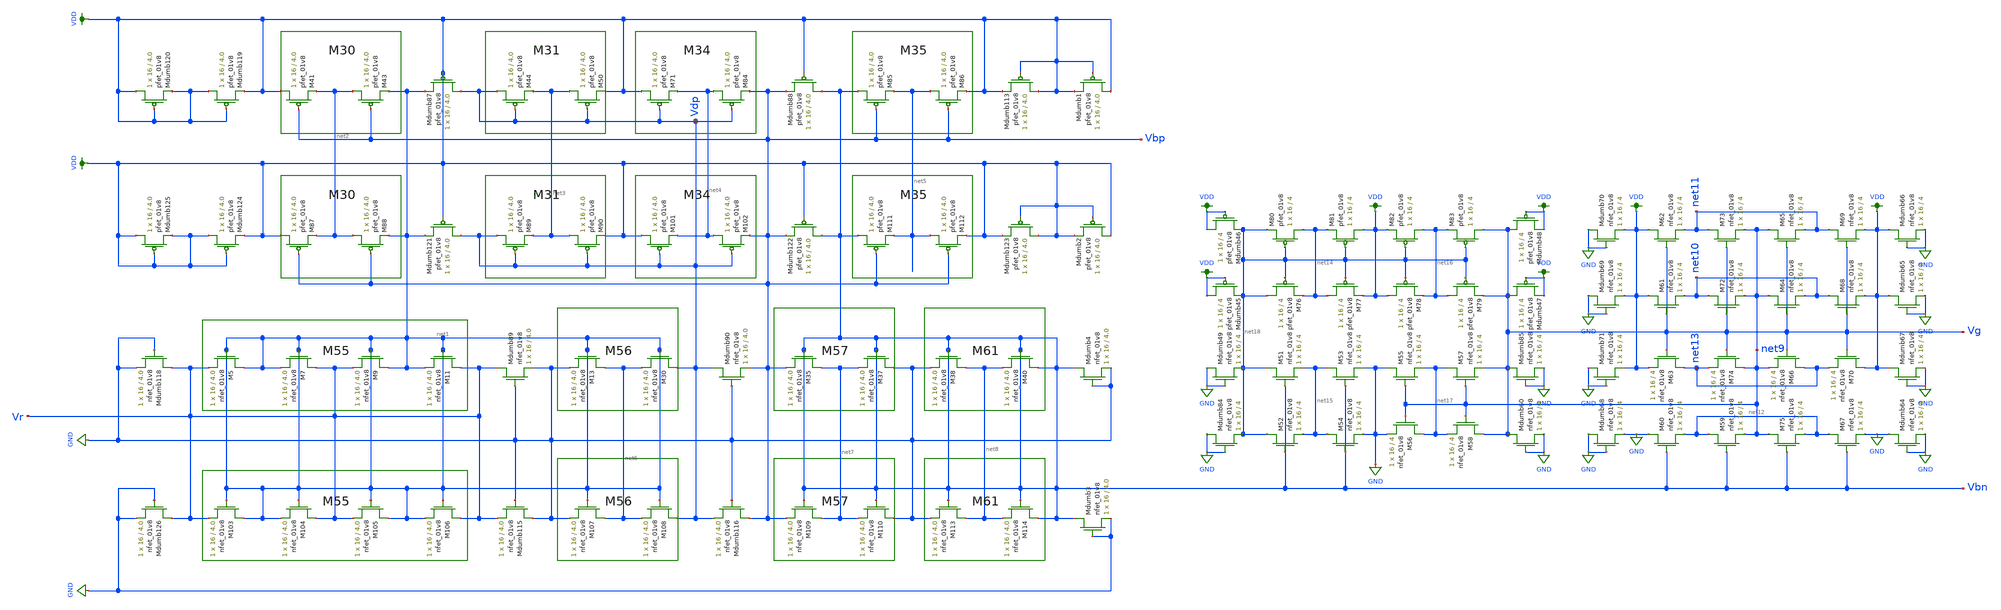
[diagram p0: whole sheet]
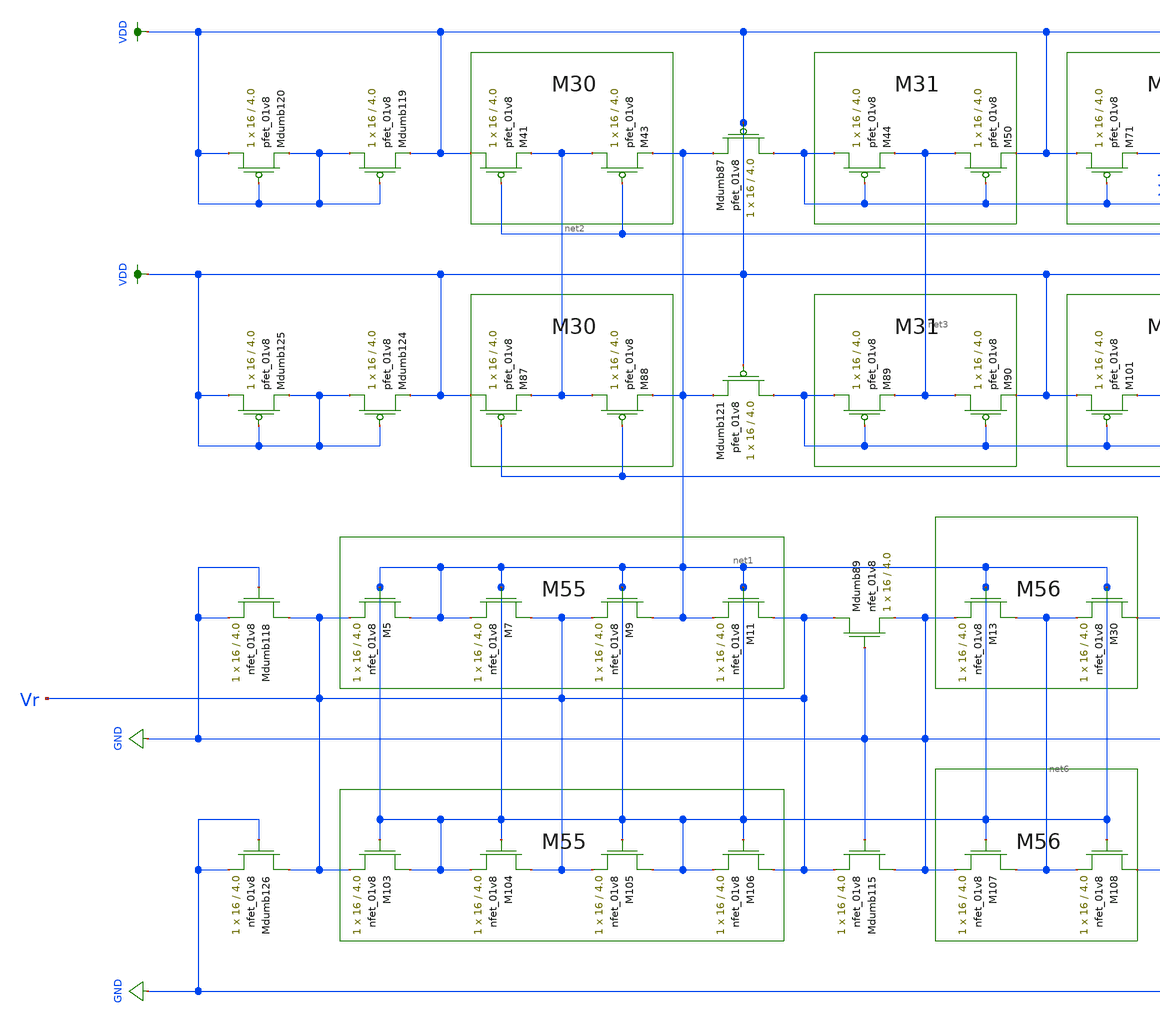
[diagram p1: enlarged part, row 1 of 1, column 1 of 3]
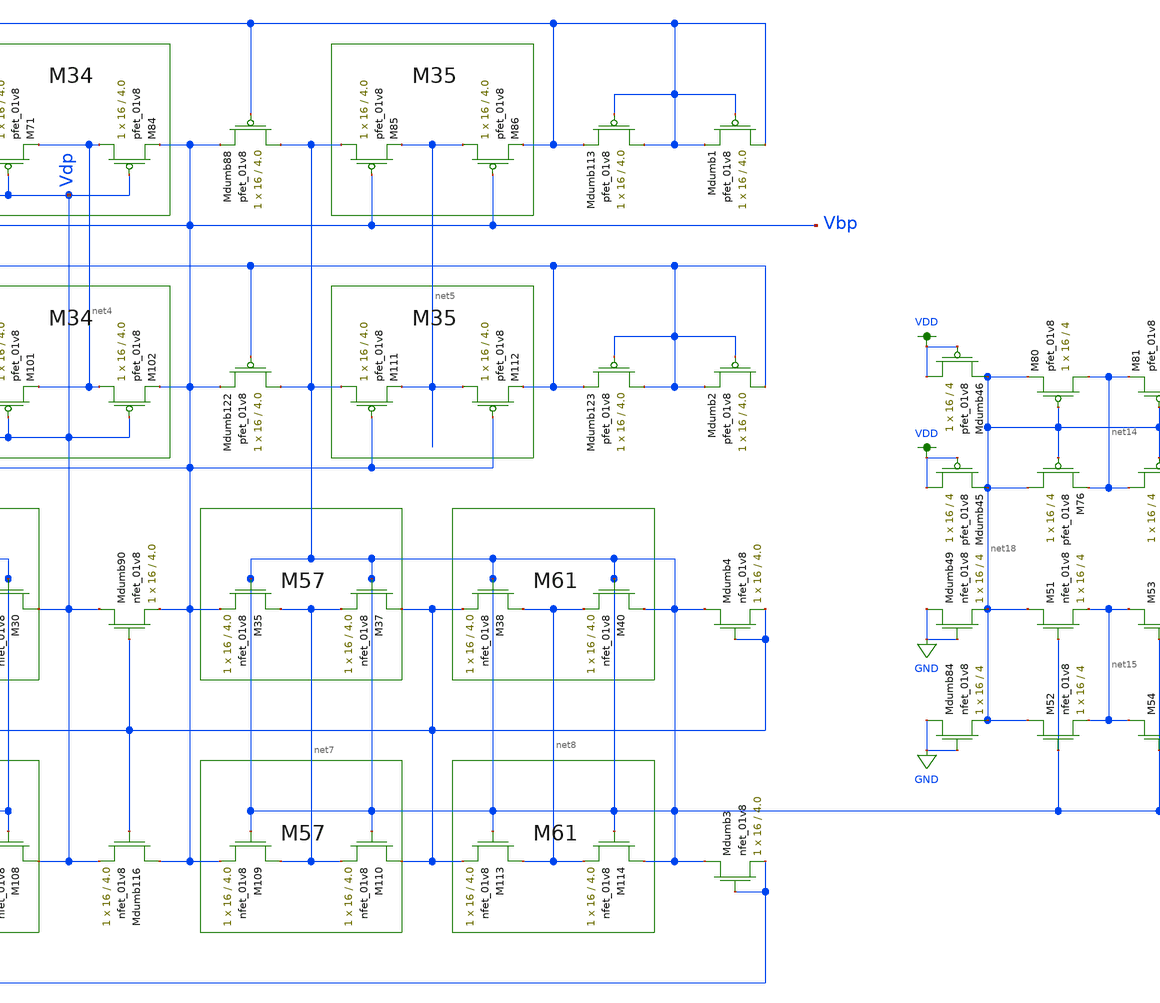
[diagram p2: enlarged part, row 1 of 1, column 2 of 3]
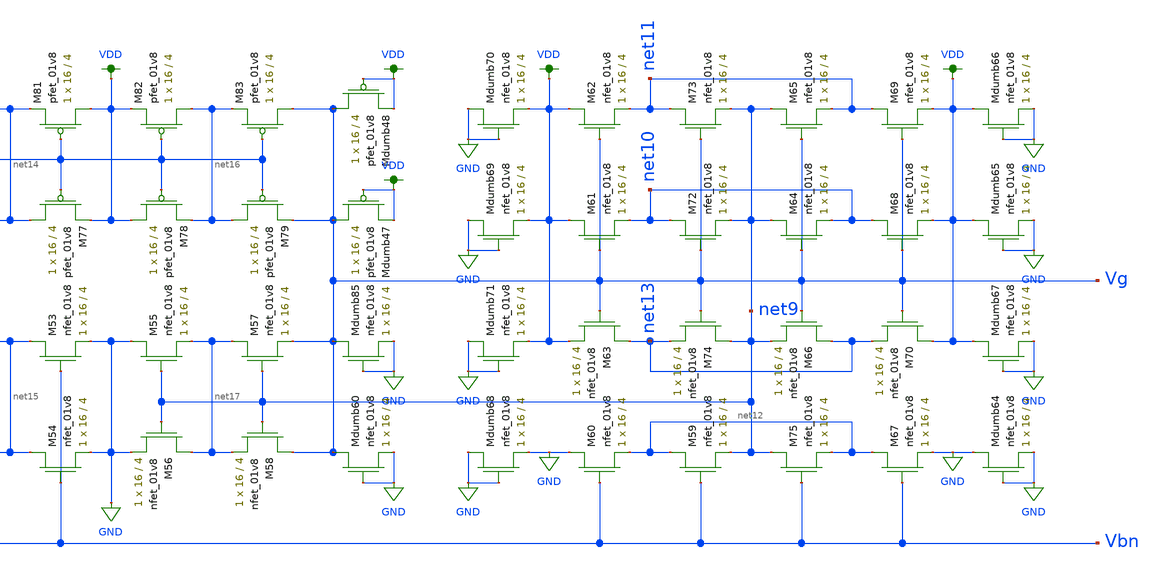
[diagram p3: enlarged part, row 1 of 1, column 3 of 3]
** sch_path: schematic/LDS/ibias_vg_lvs.sch
**.subckt ibias_vg_lvs
XM5 net1 net1 Vr GND sky130_fd_pr__nfet_01v8 L=4.0 W=16 nf=1 ad='int((nf+1)/2) * W/nf * 0.29' as='int((nf+2)/2) * W/nf * 0.29'
+ pd='2*int((nf+1)/2) * (W/nf + 0.29)' ps='2*int((nf+2)/2) * (W/nf + 0.29)' nrd='0.29 / W' nrs='0.29 / W'
+ sa=0 sb=0 sd=0 mult=1 m=1
XM7 Vr net1 net1 GND sky130_fd_pr__nfet_01v8 L=4.0 W=16 nf=1 ad='int((nf+1)/2) * W/nf * 0.29' as='int((nf+2)/2) * W/nf * 0.29'
+ pd='2*int((nf+1)/2) * (W/nf + 0.29)' ps='2*int((nf+2)/2) * (W/nf + 0.29)' nrd='0.29 / W' nrs='0.29 / W'
+ sa=0 sb=0 sd=0 mult=1 m=1
XM9 net1 net1 Vr GND sky130_fd_pr__nfet_01v8 L=4.0 W=16 nf=1 ad='int((nf+1)/2) * W/nf * 0.29' as='int((nf+2)/2) * W/nf * 0.29'
+ pd='2*int((nf+1)/2) * (W/nf + 0.29)' ps='2*int((nf+2)/2) * (W/nf + 0.29)' nrd='0.29 / W' nrs='0.29 / W'
+ sa=0 sb=0 sd=0 mult=1 m=1
XM11 Vr net1 net1 GND sky130_fd_pr__nfet_01v8 L=4.0 W=16 nf=1 ad='int((nf+1)/2) * W/nf * 0.29' as='int((nf+2)/2) * W/nf * 0.29'
+ pd='2*int((nf+1)/2) * (W/nf + 0.29)' ps='2*int((nf+2)/2) * (W/nf + 0.29)' nrd='0.29 / W' nrs='0.29 / W'
+ sa=0 sb=0 sd=0 mult=1 m=1
XM13 net6 net1 GND GND sky130_fd_pr__nfet_01v8 L=4.0 W=16 nf=1 ad='int((nf+1)/2) * W/nf * 0.29' as='int((nf+2)/2) * W/nf * 0.29'
+ pd='2*int((nf+1)/2) * (W/nf + 0.29)' ps='2*int((nf+2)/2) * (W/nf + 0.29)' nrd='0.29 / W' nrs='0.29 / W'
+ sa=0 sb=0 sd=0 mult=1 m=1
XM30 Vdp net1 net6 GND sky130_fd_pr__nfet_01v8 L=4.0 W=16 nf=1 ad='int((nf+1)/2) * W/nf * 0.29' as='int((nf+2)/2) * W/nf * 0.29'
+ pd='2*int((nf+1)/2) * (W/nf + 0.29)' ps='2*int((nf+2)/2) * (W/nf + 0.29)' nrd='0.29 / W' nrs='0.29 / W'
+ sa=0 sb=0 sd=0 mult=1 m=1
XM35 net7 Vbn Vbp GND sky130_fd_pr__nfet_01v8 L=4.0 W=16 nf=1 ad='int((nf+1)/2) * W/nf * 0.29' as='int((nf+2)/2) * W/nf * 0.29'
+ pd='2*int((nf+1)/2) * (W/nf + 0.29)' ps='2*int((nf+2)/2) * (W/nf + 0.29)' nrd='0.29 / W' nrs='0.29 / W'
+ sa=0 sb=0 sd=0 mult=1 m=1
XM37 GND Vbn net7 GND sky130_fd_pr__nfet_01v8 L=4.0 W=16 nf=1 ad='int((nf+1)/2) * W/nf * 0.29' as='int((nf+2)/2) * W/nf * 0.29'
+ pd='2*int((nf+1)/2) * (W/nf + 0.29)' ps='2*int((nf+2)/2) * (W/nf + 0.29)' nrd='0.29 / W' nrs='0.29 / W'
+ sa=0 sb=0 sd=0 mult=1 m=1
XM38 net8 Vbn GND GND sky130_fd_pr__nfet_01v8 L=4.0 W=16 nf=1 ad='int((nf+1)/2) * W/nf * 0.29' as='int((nf+2)/2) * W/nf * 0.29'
+ pd='2*int((nf+1)/2) * (W/nf + 0.29)' ps='2*int((nf+2)/2) * (W/nf + 0.29)' nrd='0.29 / W' nrs='0.29 / W'
+ sa=0 sb=0 sd=0 mult=1 m=1
XM40 Vbn Vbn net8 GND sky130_fd_pr__nfet_01v8 L=4.0 W=16 nf=1 ad='int((nf+1)/2) * W/nf * 0.29' as='int((nf+2)/2) * W/nf * 0.29'
+ pd='2*int((nf+1)/2) * (W/nf + 0.29)' ps='2*int((nf+2)/2) * (W/nf + 0.29)' nrd='0.29 / W' nrs='0.29 / W'
+ sa=0 sb=0 sd=0 mult=1 m=1
XM41 VDD Vbp net2 VDD sky130_fd_pr__pfet_01v8 L=4.0 W=16 nf=1 ad='int((nf+1)/2) * W/nf * 0.29' as='int((nf+2)/2) * W/nf * 0.29'
+ pd='2*int((nf+1)/2) * (W/nf + 0.29)' ps='2*int((nf+2)/2) * (W/nf + 0.29)' nrd='0.29 / W' nrs='0.29 / W'
+ sa=0 sb=0 sd=0 mult=1 m=1
XM43 net2 Vbp net1 VDD sky130_fd_pr__pfet_01v8 L=4.0 W=16 nf=1 ad='int((nf+1)/2) * W/nf * 0.29' as='int((nf+2)/2) * W/nf * 0.29'
+ pd='2*int((nf+1)/2) * (W/nf + 0.29)' ps='2*int((nf+2)/2) * (W/nf + 0.29)' nrd='0.29 / W' nrs='0.29 / W'
+ sa=0 sb=0 sd=0 mult=1 m=1
XM44 Vdp Vdp net3 VDD sky130_fd_pr__pfet_01v8 L=4.0 W=16 nf=1 ad='int((nf+1)/2) * W/nf * 0.29' as='int((nf+2)/2) * W/nf * 0.29'
+ pd='2*int((nf+1)/2) * (W/nf + 0.29)' ps='2*int((nf+2)/2) * (W/nf + 0.29)' nrd='0.29 / W' nrs='0.29 / W'
+ sa=0 sb=0 sd=0 mult=1 m=1
XM50 net3 Vdp VDD VDD sky130_fd_pr__pfet_01v8 L=4.0 W=16 nf=1 ad='int((nf+1)/2) * W/nf * 0.29' as='int((nf+2)/2) * W/nf * 0.29'
+ pd='2*int((nf+1)/2) * (W/nf + 0.29)' ps='2*int((nf+2)/2) * (W/nf + 0.29)' nrd='0.29 / W' nrs='0.29 / W'
+ sa=0 sb=0 sd=0 mult=1 m=1
XM71 VDD Vdp net4 VDD sky130_fd_pr__pfet_01v8 L=4.0 W=16 nf=1 ad='int((nf+1)/2) * W/nf * 0.29' as='int((nf+2)/2) * W/nf * 0.29'
+ pd='2*int((nf+1)/2) * (W/nf + 0.29)' ps='2*int((nf+2)/2) * (W/nf + 0.29)' nrd='0.29 / W' nrs='0.29 / W'
+ sa=0 sb=0 sd=0 mult=1 m=1
XM84 net4 Vdp Vbp VDD sky130_fd_pr__pfet_01v8 L=4.0 W=16 nf=1 ad='int((nf+1)/2) * W/nf * 0.29' as='int((nf+2)/2) * W/nf * 0.29'
+ pd='2*int((nf+1)/2) * (W/nf + 0.29)' ps='2*int((nf+2)/2) * (W/nf + 0.29)' nrd='0.29 / W' nrs='0.29 / W'
+ sa=0 sb=0 sd=0 mult=1 m=1
XM85 Vbn Vbp net5 VDD sky130_fd_pr__pfet_01v8 L=4.0 W=16 nf=1 ad='int((nf+1)/2) * W/nf * 0.29' as='int((nf+2)/2) * W/nf * 0.29'
+ pd='2*int((nf+1)/2) * (W/nf + 0.29)' ps='2*int((nf+2)/2) * (W/nf + 0.29)' nrd='0.29 / W' nrs='0.29 / W'
+ sa=0 sb=0 sd=0 mult=1 m=1
XM86 net5 Vbp VDD VDD sky130_fd_pr__pfet_01v8 L=4.0 W=16 nf=1 ad='int((nf+1)/2) * W/nf * 0.29' as='int((nf+2)/2) * W/nf * 0.29'
+ pd='2*int((nf+1)/2) * (W/nf + 0.29)' ps='2*int((nf+2)/2) * (W/nf + 0.29)' nrd='0.29 / W' nrs='0.29 / W'
+ sa=0 sb=0 sd=0 mult=1 m=1
XMdumb87 Vdp VDD net1 VDD sky130_fd_pr__pfet_01v8 L=4.0 W=16 nf=1 ad='int((nf+1)/2) * W/nf * 0.29' as='int((nf+2)/2) * W/nf * 0.29'
+ pd='2*int((nf+1)/2) * (W/nf + 0.29)' ps='2*int((nf+2)/2) * (W/nf + 0.29)' nrd='0.29 / W' nrs='0.29 / W'
+ sa=0 sb=0 sd=0 mult=1 m=1
XMdumb88 Vbn VDD Vbp VDD sky130_fd_pr__pfet_01v8 L=4.0 W=16 nf=1 ad='int((nf+1)/2) * W/nf * 0.29' as='int((nf+2)/2) * W/nf * 0.29'
+ pd='2*int((nf+1)/2) * (W/nf + 0.29)' ps='2*int((nf+2)/2) * (W/nf + 0.29)' nrd='0.29 / W' nrs='0.29 / W'
+ sa=0 sb=0 sd=0 mult=1 m=1
XMdumb89 Vr GND GND GND sky130_fd_pr__nfet_01v8 L=4.0 W=16 nf=1 ad='int((nf+1)/2) * W/nf * 0.29' as='int((nf+2)/2) * W/nf * 0.29'
+ pd='2*int((nf+1)/2) * (W/nf + 0.29)' ps='2*int((nf+2)/2) * (W/nf + 0.29)' nrd='0.29 / W' nrs='0.29 / W'
+ sa=0 sb=0 sd=0 mult=1 m=1
XMdumb90 Vdp GND Vbp GND sky130_fd_pr__nfet_01v8 L=4.0 W=16 nf=1 ad='int((nf+1)/2) * W/nf * 0.29' as='int((nf+2)/2) * W/nf * 0.29'
+ pd='2*int((nf+1)/2) * (W/nf + 0.29)' ps='2*int((nf+2)/2) * (W/nf + 0.29)' nrd='0.29 / W' nrs='0.29 / W'
+ sa=0 sb=0 sd=0 mult=1 m=1
XMdumb113 VDD VDD VDD VDD sky130_fd_pr__pfet_01v8 L=4.0 W=16 nf=1 ad='int((nf+1)/2) * W/nf * 0.29' as='int((nf+2)/2) * W/nf * 0.29'
+ pd='2*int((nf+1)/2) * (W/nf + 0.29)' ps='2*int((nf+2)/2) * (W/nf + 0.29)' nrd='0.29 / W' nrs='0.29 / W'
+ sa=0 sb=0 sd=0 mult=1 m=1
XMdumb118 Vr GND GND GND sky130_fd_pr__nfet_01v8 L=4.0 W=16 nf=1 ad='int((nf+1)/2) * W/nf * 0.29' as='int((nf+2)/2) * W/nf * 0.29'
+ pd='2*int((nf+1)/2) * (W/nf + 0.29)' ps='2*int((nf+2)/2) * (W/nf + 0.29)' nrd='0.29 / W' nrs='0.29 / W'
+ sa=0 sb=0 sd=0 mult=1 m=1
XMdumb119 VDD VDD VDD VDD sky130_fd_pr__pfet_01v8 L=4.0 W=16 nf=1 ad='int((nf+1)/2) * W/nf * 0.29' as='int((nf+2)/2) * W/nf * 0.29'
+ pd='2*int((nf+1)/2) * (W/nf + 0.29)' ps='2*int((nf+2)/2) * (W/nf + 0.29)' nrd='0.29 / W' nrs='0.29 / W'
+ sa=0 sb=0 sd=0 mult=1 m=1
XMdumb120 VDD VDD VDD VDD sky130_fd_pr__pfet_01v8 L=4.0 W=16 nf=1 ad='int((nf+1)/2) * W/nf * 0.29' as='int((nf+2)/2) * W/nf * 0.29'
+ pd='2*int((nf+1)/2) * (W/nf + 0.29)' ps='2*int((nf+2)/2) * (W/nf + 0.29)' nrd='0.29 / W' nrs='0.29 / W'
+ sa=0 sb=0 sd=0 mult=1 m=1
XM87 VDD Vbp net2 VDD sky130_fd_pr__pfet_01v8 L=4.0 W=16 nf=1 ad='int((nf+1)/2) * W/nf * 0.29' as='int((nf+2)/2) * W/nf * 0.29'
+ pd='2*int((nf+1)/2) * (W/nf + 0.29)' ps='2*int((nf+2)/2) * (W/nf + 0.29)' nrd='0.29 / W' nrs='0.29 / W'
+ sa=0 sb=0 sd=0 mult=1 m=1
XM88 net2 Vbp net1 VDD sky130_fd_pr__pfet_01v8 L=4.0 W=16 nf=1 ad='int((nf+1)/2) * W/nf * 0.29' as='int((nf+2)/2) * W/nf * 0.29'
+ pd='2*int((nf+1)/2) * (W/nf + 0.29)' ps='2*int((nf+2)/2) * (W/nf + 0.29)' nrd='0.29 / W' nrs='0.29 / W'
+ sa=0 sb=0 sd=0 mult=1 m=1
XM89 Vdp Vdp net3 VDD sky130_fd_pr__pfet_01v8 L=4.0 W=16 nf=1 ad='int((nf+1)/2) * W/nf * 0.29' as='int((nf+2)/2) * W/nf * 0.29'
+ pd='2*int((nf+1)/2) * (W/nf + 0.29)' ps='2*int((nf+2)/2) * (W/nf + 0.29)' nrd='0.29 / W' nrs='0.29 / W'
+ sa=0 sb=0 sd=0 mult=1 m=1
XM90 net3 Vdp VDD VDD sky130_fd_pr__pfet_01v8 L=4.0 W=16 nf=1 ad='int((nf+1)/2) * W/nf * 0.29' as='int((nf+2)/2) * W/nf * 0.29'
+ pd='2*int((nf+1)/2) * (W/nf + 0.29)' ps='2*int((nf+2)/2) * (W/nf + 0.29)' nrd='0.29 / W' nrs='0.29 / W'
+ sa=0 sb=0 sd=0 mult=1 m=1
XM101 VDD Vdp net4 VDD sky130_fd_pr__pfet_01v8 L=4.0 W=16 nf=1 ad='int((nf+1)/2) * W/nf * 0.29' as='int((nf+2)/2) * W/nf * 0.29'
+ pd='2*int((nf+1)/2) * (W/nf + 0.29)' ps='2*int((nf+2)/2) * (W/nf + 0.29)' nrd='0.29 / W' nrs='0.29 / W'
+ sa=0 sb=0 sd=0 mult=1 m=1
XM102 net4 Vdp Vbp VDD sky130_fd_pr__pfet_01v8 L=4.0 W=16 nf=1 ad='int((nf+1)/2) * W/nf * 0.29' as='int((nf+2)/2) * W/nf * 0.29'
+ pd='2*int((nf+1)/2) * (W/nf + 0.29)' ps='2*int((nf+2)/2) * (W/nf + 0.29)' nrd='0.29 / W' nrs='0.29 / W'
+ sa=0 sb=0 sd=0 mult=1 m=1
XM111 Vbn Vbp net5 VDD sky130_fd_pr__pfet_01v8 L=4.0 W=16 nf=1 ad='int((nf+1)/2) * W/nf * 0.29' as='int((nf+2)/2) * W/nf * 0.29'
+ pd='2*int((nf+1)/2) * (W/nf + 0.29)' ps='2*int((nf+2)/2) * (W/nf + 0.29)' nrd='0.29 / W' nrs='0.29 / W'
+ sa=0 sb=0 sd=0 mult=1 m=1
XM112 net5 Vbp VDD VDD sky130_fd_pr__pfet_01v8 L=4.0 W=16 nf=1 ad='int((nf+1)/2) * W/nf * 0.29' as='int((nf+2)/2) * W/nf * 0.29'
+ pd='2*int((nf+1)/2) * (W/nf + 0.29)' ps='2*int((nf+2)/2) * (W/nf + 0.29)' nrd='0.29 / W' nrs='0.29 / W'
+ sa=0 sb=0 sd=0 mult=1 m=1
XMdumb121 Vdp VDD net1 VDD sky130_fd_pr__pfet_01v8 L=4.0 W=16 nf=1 ad='int((nf+1)/2) * W/nf * 0.29' as='int((nf+2)/2) * W/nf * 0.29'
+ pd='2*int((nf+1)/2) * (W/nf + 0.29)' ps='2*int((nf+2)/2) * (W/nf + 0.29)' nrd='0.29 / W' nrs='0.29 / W'
+ sa=0 sb=0 sd=0 mult=1 m=1
XMdumb122 Vbn VDD Vbp VDD sky130_fd_pr__pfet_01v8 L=4.0 W=16 nf=1 ad='int((nf+1)/2) * W/nf * 0.29' as='int((nf+2)/2) * W/nf * 0.29'
+ pd='2*int((nf+1)/2) * (W/nf + 0.29)' ps='2*int((nf+2)/2) * (W/nf + 0.29)' nrd='0.29 / W' nrs='0.29 / W'
+ sa=0 sb=0 sd=0 mult=1 m=1
XMdumb123 VDD VDD VDD VDD sky130_fd_pr__pfet_01v8 L=4.0 W=16 nf=1 ad='int((nf+1)/2) * W/nf * 0.29' as='int((nf+2)/2) * W/nf * 0.29'
+ pd='2*int((nf+1)/2) * (W/nf + 0.29)' ps='2*int((nf+2)/2) * (W/nf + 0.29)' nrd='0.29 / W' nrs='0.29 / W'
+ sa=0 sb=0 sd=0 mult=1 m=1
XMdumb124 VDD VDD VDD VDD sky130_fd_pr__pfet_01v8 L=4.0 W=16 nf=1 ad='int((nf+1)/2) * W/nf * 0.29' as='int((nf+2)/2) * W/nf * 0.29'
+ pd='2*int((nf+1)/2) * (W/nf + 0.29)' ps='2*int((nf+2)/2) * (W/nf + 0.29)' nrd='0.29 / W' nrs='0.29 / W'
+ sa=0 sb=0 sd=0 mult=1 m=1
XMdumb125 VDD VDD VDD VDD sky130_fd_pr__pfet_01v8 L=4.0 W=16 nf=1 ad='int((nf+1)/2) * W/nf * 0.29' as='int((nf+2)/2) * W/nf * 0.29'
+ pd='2*int((nf+1)/2) * (W/nf + 0.29)' ps='2*int((nf+2)/2) * (W/nf + 0.29)' nrd='0.29 / W' nrs='0.29 / W'
+ sa=0 sb=0 sd=0 mult=1 m=1
XM103 net1 net1 Vr GND sky130_fd_pr__nfet_01v8 L=4.0 W=16 nf=1 ad='int((nf+1)/2) * W/nf * 0.29' as='int((nf+2)/2) * W/nf * 0.29'
+ pd='2*int((nf+1)/2) * (W/nf + 0.29)' ps='2*int((nf+2)/2) * (W/nf + 0.29)' nrd='0.29 / W' nrs='0.29 / W'
+ sa=0 sb=0 sd=0 mult=1 m=1
XM104 Vr net1 net1 GND sky130_fd_pr__nfet_01v8 L=4.0 W=16 nf=1 ad='int((nf+1)/2) * W/nf * 0.29' as='int((nf+2)/2) * W/nf * 0.29'
+ pd='2*int((nf+1)/2) * (W/nf + 0.29)' ps='2*int((nf+2)/2) * (W/nf + 0.29)' nrd='0.29 / W' nrs='0.29 / W'
+ sa=0 sb=0 sd=0 mult=1 m=1
XM105 net1 net1 Vr GND sky130_fd_pr__nfet_01v8 L=4.0 W=16 nf=1 ad='int((nf+1)/2) * W/nf * 0.29' as='int((nf+2)/2) * W/nf * 0.29'
+ pd='2*int((nf+1)/2) * (W/nf + 0.29)' ps='2*int((nf+2)/2) * (W/nf + 0.29)' nrd='0.29 / W' nrs='0.29 / W'
+ sa=0 sb=0 sd=0 mult=1 m=1
XM106 Vr net1 net1 GND sky130_fd_pr__nfet_01v8 L=4.0 W=16 nf=1 ad='int((nf+1)/2) * W/nf * 0.29' as='int((nf+2)/2) * W/nf * 0.29'
+ pd='2*int((nf+1)/2) * (W/nf + 0.29)' ps='2*int((nf+2)/2) * (W/nf + 0.29)' nrd='0.29 / W' nrs='0.29 / W'
+ sa=0 sb=0 sd=0 mult=1 m=1
XM107 net6 net1 GND GND sky130_fd_pr__nfet_01v8 L=4.0 W=16 nf=1 ad='int((nf+1)/2) * W/nf * 0.29' as='int((nf+2)/2) * W/nf * 0.29'
+ pd='2*int((nf+1)/2) * (W/nf + 0.29)' ps='2*int((nf+2)/2) * (W/nf + 0.29)' nrd='0.29 / W' nrs='0.29 / W'
+ sa=0 sb=0 sd=0 mult=1 m=1
XM108 Vdp net1 net6 GND sky130_fd_pr__nfet_01v8 L=4.0 W=16 nf=1 ad='int((nf+1)/2) * W/nf * 0.29' as='int((nf+2)/2) * W/nf * 0.29'
+ pd='2*int((nf+1)/2) * (W/nf + 0.29)' ps='2*int((nf+2)/2) * (W/nf + 0.29)' nrd='0.29 / W' nrs='0.29 / W'
+ sa=0 sb=0 sd=0 mult=1 m=1
XM109 net7 Vbn Vbp GND sky130_fd_pr__nfet_01v8 L=4.0 W=16 nf=1 ad='int((nf+1)/2) * W/nf * 0.29' as='int((nf+2)/2) * W/nf * 0.29'
+ pd='2*int((nf+1)/2) * (W/nf + 0.29)' ps='2*int((nf+2)/2) * (W/nf + 0.29)' nrd='0.29 / W' nrs='0.29 / W'
+ sa=0 sb=0 sd=0 mult=1 m=1
XM110 GND Vbn net7 GND sky130_fd_pr__nfet_01v8 L=4.0 W=16 nf=1 ad='int((nf+1)/2) * W/nf * 0.29' as='int((nf+2)/2) * W/nf * 0.29'
+ pd='2*int((nf+1)/2) * (W/nf + 0.29)' ps='2*int((nf+2)/2) * (W/nf + 0.29)' nrd='0.29 / W' nrs='0.29 / W'
+ sa=0 sb=0 sd=0 mult=1 m=1
XM113 net8 Vbn GND GND sky130_fd_pr__nfet_01v8 L=4.0 W=16 nf=1 ad='int((nf+1)/2) * W/nf * 0.29' as='int((nf+2)/2) * W/nf * 0.29'
+ pd='2*int((nf+1)/2) * (W/nf + 0.29)' ps='2*int((nf+2)/2) * (W/nf + 0.29)' nrd='0.29 / W' nrs='0.29 / W'
+ sa=0 sb=0 sd=0 mult=1 m=1
XM114 Vbn Vbn net8 GND sky130_fd_pr__nfet_01v8 L=4.0 W=16 nf=1 ad='int((nf+1)/2) * W/nf * 0.29' as='int((nf+2)/2) * W/nf * 0.29'
+ pd='2*int((nf+1)/2) * (W/nf + 0.29)' ps='2*int((nf+2)/2) * (W/nf + 0.29)' nrd='0.29 / W' nrs='0.29 / W'
+ sa=0 sb=0 sd=0 mult=1 m=1
XMdumb115 GND GND Vr GND sky130_fd_pr__nfet_01v8 L=4.0 W=16 nf=1 ad='int((nf+1)/2) * W/nf * 0.29' as='int((nf+2)/2) * W/nf * 0.29'
+ pd='2*int((nf+1)/2) * (W/nf + 0.29)' ps='2*int((nf+2)/2) * (W/nf + 0.29)' nrd='0.29 / W' nrs='0.29 / W'
+ sa=0 sb=0 sd=0 mult=1 m=1
XMdumb116 Vbp GND Vdp GND sky130_fd_pr__nfet_01v8 L=4.0 W=16 nf=1 ad='int((nf+1)/2) * W/nf * 0.29' as='int((nf+2)/2) * W/nf * 0.29'
+ pd='2*int((nf+1)/2) * (W/nf + 0.29)' ps='2*int((nf+2)/2) * (W/nf + 0.29)' nrd='0.29 / W' nrs='0.29 / W'
+ sa=0 sb=0 sd=0 mult=1 m=1
XMdumb126 Vr GND GND GND sky130_fd_pr__nfet_01v8 L=4.0 W=16 nf=1 ad='int((nf+1)/2) * W/nf * 0.29' as='int((nf+2)/2) * W/nf * 0.29'
+ pd='2*int((nf+1)/2) * (W/nf + 0.29)' ps='2*int((nf+2)/2) * (W/nf + 0.29)' nrd='0.29 / W' nrs='0.29 / W'
+ sa=0 sb=0 sd=0 mult=1 m=1
XMdumb1 VDD VDD VDD VDD sky130_fd_pr__pfet_01v8 L=4.0 W=16 nf=1 ad='int((nf+1)/2) * W/nf * 0.29' as='int((nf+2)/2) * W/nf * 0.29'
+ pd='2*int((nf+1)/2) * (W/nf + 0.29)' ps='2*int((nf+2)/2) * (W/nf + 0.29)' nrd='0.29 / W' nrs='0.29 / W'
+ sa=0 sb=0 sd=0 mult=1 m=1
XMdumb2 VDD VDD VDD VDD sky130_fd_pr__pfet_01v8 L=4.0 W=16 nf=1 ad='int((nf+1)/2) * W/nf * 0.29' as='int((nf+2)/2) * W/nf * 0.29'
+ pd='2*int((nf+1)/2) * (W/nf + 0.29)' ps='2*int((nf+2)/2) * (W/nf + 0.29)' nrd='0.29 / W' nrs='0.29 / W'
+ sa=0 sb=0 sd=0 mult=1 m=1
XMdumb3 Vbn GND GND GND sky130_fd_pr__nfet_01v8 L=4.0 W=16 nf=1 ad='int((nf+1)/2) * W/nf * 0.29' as='int((nf+2)/2) * W/nf * 0.29'
+ pd='2*int((nf+1)/2) * (W/nf + 0.29)' ps='2*int((nf+2)/2) * (W/nf + 0.29)' nrd='0.29 / W' nrs='0.29 / W'
+ sa=0 sb=0 sd=0 mult=1 m=1
XMdumb4 Vbn GND GND GND sky130_fd_pr__nfet_01v8 L=4.0 W=16 nf=1 ad='int((nf+1)/2) * W/nf * 0.29' as='int((nf+2)/2) * W/nf * 0.29'
+ pd='2*int((nf+1)/2) * (W/nf + 0.29)' ps='2*int((nf+2)/2) * (W/nf + 0.29)' nrd='0.29 / W' nrs='0.29 / W'
+ sa=0 sb=0 sd=0 mult=1 m=1
XM60 GND Vbn net12 GND sky130_fd_pr__nfet_01v8 L=4 W=16 nf=1 ad='int((nf+1)/2) * W/nf * 0.29' as='int((nf+2)/2) * W/nf * 0.29'
+ pd='2*int((nf+1)/2) * (W/nf + 0.29)' ps='2*int((nf+2)/2) * (W/nf + 0.29)' nrd='0.29 / W' nrs='0.29 / W'
+ sa=0 sb=0 sd=0 mult=1 m=1
XM61 VDD Vg net10 GND sky130_fd_pr__nfet_01v8 L=4 W=16 nf=1 ad='int((nf+1)/2) * W/nf * 0.29' as='int((nf+2)/2) * W/nf * 0.29'
+ pd='2*int((nf+1)/2) * (W/nf + 0.29)' ps='2*int((nf+2)/2) * (W/nf + 0.29)' nrd='0.29 / W' nrs='0.29 / W'
+ sa=0 sb=0 sd=0 mult=1 m=1
XM62 VDD Vg net11 GND sky130_fd_pr__nfet_01v8 L=4 W=16 nf=1 ad='int((nf+1)/2) * W/nf * 0.29' as='int((nf+2)/2) * W/nf * 0.29'
+ pd='2*int((nf+1)/2) * (W/nf + 0.29)' ps='2*int((nf+2)/2) * (W/nf + 0.29)' nrd='0.29 / W' nrs='0.29 / W'
+ sa=0 sb=0 sd=0 mult=1 m=1
XM63 net13 Vg VDD GND sky130_fd_pr__nfet_01v8 L=4 W=16 nf=1 ad='int((nf+1)/2) * W/nf * 0.29' as='int((nf+2)/2) * W/nf * 0.29'
+ pd='2*int((nf+1)/2) * (W/nf + 0.29)' ps='2*int((nf+2)/2) * (W/nf + 0.29)' nrd='0.29 / W' nrs='0.29 / W'
+ sa=0 sb=0 sd=0 mult=1 m=1
XMdumb64 GND GND GND GND sky130_fd_pr__nfet_01v8 L=4 W=16 nf=1 ad='int((nf+1)/2) * W/nf * 0.29' as='int((nf+2)/2) * W/nf * 0.29'
+ pd='2*int((nf+1)/2) * (W/nf + 0.29)' ps='2*int((nf+2)/2) * (W/nf + 0.29)' nrd='0.29 / W' nrs='0.29 / W'
+ sa=0 sb=0 sd=0 mult=1 m=1
XMdumb65 VDD GND GND GND sky130_fd_pr__nfet_01v8 L=4 W=16 nf=1 ad='int((nf+1)/2) * W/nf * 0.29' as='int((nf+2)/2) * W/nf * 0.29'
+ pd='2*int((nf+1)/2) * (W/nf + 0.29)' ps='2*int((nf+2)/2) * (W/nf + 0.29)' nrd='0.29 / W' nrs='0.29 / W'
+ sa=0 sb=0 sd=0 mult=1 m=1
XMdumb66 VDD GND GND GND sky130_fd_pr__nfet_01v8 L=4 W=16 nf=1 ad='int((nf+1)/2) * W/nf * 0.29' as='int((nf+2)/2) * W/nf * 0.29'
+ pd='2*int((nf+1)/2) * (W/nf + 0.29)' ps='2*int((nf+2)/2) * (W/nf + 0.29)' nrd='0.29 / W' nrs='0.29 / W'
+ sa=0 sb=0 sd=0 mult=1 m=1
XMdumb67 VDD GND GND GND sky130_fd_pr__nfet_01v8 L=4 W=16 nf=1 ad='int((nf+1)/2) * W/nf * 0.29' as='int((nf+2)/2) * W/nf * 0.29'
+ pd='2*int((nf+1)/2) * (W/nf + 0.29)' ps='2*int((nf+2)/2) * (W/nf + 0.29)' nrd='0.29 / W' nrs='0.29 / W'
+ sa=0 sb=0 sd=0 mult=1 m=1
XMdumb68 GND GND GND GND sky130_fd_pr__nfet_01v8 L=4 W=16 nf=1 ad='int((nf+1)/2) * W/nf * 0.29' as='int((nf+2)/2) * W/nf * 0.29'
+ pd='2*int((nf+1)/2) * (W/nf + 0.29)' ps='2*int((nf+2)/2) * (W/nf + 0.29)' nrd='0.29 / W' nrs='0.29 / W'
+ sa=0 sb=0 sd=0 mult=1 m=1
XMdumb69 GND GND VDD GND sky130_fd_pr__nfet_01v8 L=4 W=16 nf=1 ad='int((nf+1)/2) * W/nf * 0.29' as='int((nf+2)/2) * W/nf * 0.29'
+ pd='2*int((nf+1)/2) * (W/nf + 0.29)' ps='2*int((nf+2)/2) * (W/nf + 0.29)' nrd='0.29 / W' nrs='0.29 / W'
+ sa=0 sb=0 sd=0 mult=1 m=1
XMdumb70 GND GND VDD GND sky130_fd_pr__nfet_01v8 L=4 W=16 nf=1 ad='int((nf+1)/2) * W/nf * 0.29' as='int((nf+2)/2) * W/nf * 0.29'
+ pd='2*int((nf+1)/2) * (W/nf + 0.29)' ps='2*int((nf+2)/2) * (W/nf + 0.29)' nrd='0.29 / W' nrs='0.29 / W'
+ sa=0 sb=0 sd=0 mult=1 m=1
XMdumb71 GND GND VDD GND sky130_fd_pr__nfet_01v8 L=4 W=16 nf=1 ad='int((nf+1)/2) * W/nf * 0.29' as='int((nf+2)/2) * W/nf * 0.29'
+ pd='2*int((nf+1)/2) * (W/nf + 0.29)' ps='2*int((nf+2)/2) * (W/nf + 0.29)' nrd='0.29 / W' nrs='0.29 / W'
+ sa=0 sb=0 sd=0 mult=1 m=1
XM59 net12 Vbn net9 GND sky130_fd_pr__nfet_01v8 L=4 W=16 nf=1 ad='int((nf+1)/2) * W/nf * 0.29' as='int((nf+2)/2) * W/nf * 0.29'
+ pd='2*int((nf+1)/2) * (W/nf + 0.29)' ps='2*int((nf+2)/2) * (W/nf + 0.29)' nrd='0.29 / W' nrs='0.29 / W'
+ sa=0 sb=0 sd=0 mult=1 m=1
XM72 net10 Vg net9 GND sky130_fd_pr__nfet_01v8 L=4 W=16 nf=1 ad='int((nf+1)/2) * W/nf * 0.29' as='int((nf+2)/2) * W/nf * 0.29'
+ pd='2*int((nf+1)/2) * (W/nf + 0.29)' ps='2*int((nf+2)/2) * (W/nf + 0.29)' nrd='0.29 / W' nrs='0.29 / W'
+ sa=0 sb=0 sd=0 mult=1 m=1
XM73 net11 Vg net9 GND sky130_fd_pr__nfet_01v8 L=4 W=16 nf=1 ad='int((nf+1)/2) * W/nf * 0.29' as='int((nf+2)/2) * W/nf * 0.29'
+ pd='2*int((nf+1)/2) * (W/nf + 0.29)' ps='2*int((nf+2)/2) * (W/nf + 0.29)' nrd='0.29 / W' nrs='0.29 / W'
+ sa=0 sb=0 sd=0 mult=1 m=1
XM74 net9 Vg net13 GND sky130_fd_pr__nfet_01v8 L=4 W=16 nf=1 ad='int((nf+1)/2) * W/nf * 0.29' as='int((nf+2)/2) * W/nf * 0.29'
+ pd='2*int((nf+1)/2) * (W/nf + 0.29)' ps='2*int((nf+2)/2) * (W/nf + 0.29)' nrd='0.29 / W' nrs='0.29 / W'
+ sa=0 sb=0 sd=0 mult=1 m=1
XM75 net9 Vbn net12 GND sky130_fd_pr__nfet_01v8 L=4 W=16 nf=1 ad='int((nf+1)/2) * W/nf * 0.29' as='int((nf+2)/2) * W/nf * 0.29'
+ pd='2*int((nf+1)/2) * (W/nf + 0.29)' ps='2*int((nf+2)/2) * (W/nf + 0.29)' nrd='0.29 / W' nrs='0.29 / W'
+ sa=0 sb=0 sd=0 mult=1 m=1
XM64 net9 Vg net10 GND sky130_fd_pr__nfet_01v8 L=4 W=16 nf=1 ad='int((nf+1)/2) * W/nf * 0.29' as='int((nf+2)/2) * W/nf * 0.29'
+ pd='2*int((nf+1)/2) * (W/nf + 0.29)' ps='2*int((nf+2)/2) * (W/nf + 0.29)' nrd='0.29 / W' nrs='0.29 / W'
+ sa=0 sb=0 sd=0 mult=1 m=1
XM65 net9 Vg net11 GND sky130_fd_pr__nfet_01v8 L=4 W=16 nf=1 ad='int((nf+1)/2) * W/nf * 0.29' as='int((nf+2)/2) * W/nf * 0.29'
+ pd='2*int((nf+1)/2) * (W/nf + 0.29)' ps='2*int((nf+2)/2) * (W/nf + 0.29)' nrd='0.29 / W' nrs='0.29 / W'
+ sa=0 sb=0 sd=0 mult=1 m=1
XM66 net13 Vg net9 GND sky130_fd_pr__nfet_01v8 L=4 W=16 nf=1 ad='int((nf+1)/2) * W/nf * 0.29' as='int((nf+2)/2) * W/nf * 0.29'
+ pd='2*int((nf+1)/2) * (W/nf + 0.29)' ps='2*int((nf+2)/2) * (W/nf + 0.29)' nrd='0.29 / W' nrs='0.29 / W'
+ sa=0 sb=0 sd=0 mult=1 m=1
XM67 net12 Vbn GND GND sky130_fd_pr__nfet_01v8 L=4 W=16 nf=1 ad='int((nf+1)/2) * W/nf * 0.29' as='int((nf+2)/2) * W/nf * 0.29'
+ pd='2*int((nf+1)/2) * (W/nf + 0.29)' ps='2*int((nf+2)/2) * (W/nf + 0.29)' nrd='0.29 / W' nrs='0.29 / W'
+ sa=0 sb=0 sd=0 mult=1 m=1
XM68 net10 Vg VDD GND sky130_fd_pr__nfet_01v8 L=4 W=16 nf=1 ad='int((nf+1)/2) * W/nf * 0.29' as='int((nf+2)/2) * W/nf * 0.29'
+ pd='2*int((nf+1)/2) * (W/nf + 0.29)' ps='2*int((nf+2)/2) * (W/nf + 0.29)' nrd='0.29 / W' nrs='0.29 / W'
+ sa=0 sb=0 sd=0 mult=1 m=1
XM69 net11 Vg VDD GND sky130_fd_pr__nfet_01v8 L=4 W=16 nf=1 ad='int((nf+1)/2) * W/nf * 0.29' as='int((nf+2)/2) * W/nf * 0.29'
+ pd='2*int((nf+1)/2) * (W/nf + 0.29)' ps='2*int((nf+2)/2) * (W/nf + 0.29)' nrd='0.29 / W' nrs='0.29 / W'
+ sa=0 sb=0 sd=0 mult=1 m=1
XM70 VDD Vg net13 GND sky130_fd_pr__nfet_01v8 L=4 W=16 nf=1 ad='int((nf+1)/2) * W/nf * 0.29' as='int((nf+2)/2) * W/nf * 0.29'
+ pd='2*int((nf+1)/2) * (W/nf + 0.29)' ps='2*int((nf+2)/2) * (W/nf + 0.29)' nrd='0.29 / W' nrs='0.29 / W'
+ sa=0 sb=0 sd=0 mult=1 m=1
XM76 net18 net18 net14 VDD sky130_fd_pr__pfet_01v8 L=4 W=16 nf=1 ad='int((nf+1)/2) * W/nf * 0.29' as='int((nf+2)/2) * W/nf * 0.29'
+ pd='2*int((nf+1)/2) * (W/nf + 0.29)' ps='2*int((nf+2)/2) * (W/nf + 0.29)' nrd='0.29 / W' nrs='0.29 / W'
+ sa=0 sb=0 sd=0 mult=1 m=1
XM77 net14 net18 VDD VDD sky130_fd_pr__pfet_01v8 L=4 W=16 nf=1 ad='int((nf+1)/2) * W/nf * 0.29' as='int((nf+2)/2) * W/nf * 0.29'
+ pd='2*int((nf+1)/2) * (W/nf + 0.29)' ps='2*int((nf+2)/2) * (W/nf + 0.29)' nrd='0.29 / W' nrs='0.29 / W'
+ sa=0 sb=0 sd=0 mult=1 m=1
XM78 VDD net18 net16 VDD sky130_fd_pr__pfet_01v8 L=4 W=16 nf=1 ad='int((nf+1)/2) * W/nf * 0.29' as='int((nf+2)/2) * W/nf * 0.29'
+ pd='2*int((nf+1)/2) * (W/nf + 0.29)' ps='2*int((nf+2)/2) * (W/nf + 0.29)' nrd='0.29 / W' nrs='0.29 / W'
+ sa=0 sb=0 sd=0 mult=1 m=1
XM79 net16 net18 Vg VDD sky130_fd_pr__pfet_01v8 L=4 W=16 nf=1 ad='int((nf+1)/2) * W/nf * 0.29' as='int((nf+2)/2) * W/nf * 0.29'
+ pd='2*int((nf+1)/2) * (W/nf + 0.29)' ps='2*int((nf+2)/2) * (W/nf + 0.29)' nrd='0.29 / W' nrs='0.29 / W'
+ sa=0 sb=0 sd=0 mult=1 m=1
XM80 net14 net18 net18 VDD sky130_fd_pr__pfet_01v8 L=4 W=16 nf=1 ad='int((nf+1)/2) * W/nf * 0.29' as='int((nf+2)/2) * W/nf * 0.29'
+ pd='2*int((nf+1)/2) * (W/nf + 0.29)' ps='2*int((nf+2)/2) * (W/nf + 0.29)' nrd='0.29 / W' nrs='0.29 / W'
+ sa=0 sb=0 sd=0 mult=1 m=1
XM81 VDD net18 net14 VDD sky130_fd_pr__pfet_01v8 L=4 W=16 nf=1 ad='int((nf+1)/2) * W/nf * 0.29' as='int((nf+2)/2) * W/nf * 0.29'
+ pd='2*int((nf+1)/2) * (W/nf + 0.29)' ps='2*int((nf+2)/2) * (W/nf + 0.29)' nrd='0.29 / W' nrs='0.29 / W'
+ sa=0 sb=0 sd=0 mult=1 m=1
XM82 net16 net18 VDD VDD sky130_fd_pr__pfet_01v8 L=4 W=16 nf=1 ad='int((nf+1)/2) * W/nf * 0.29' as='int((nf+2)/2) * W/nf * 0.29'
+ pd='2*int((nf+1)/2) * (W/nf + 0.29)' ps='2*int((nf+2)/2) * (W/nf + 0.29)' nrd='0.29 / W' nrs='0.29 / W'
+ sa=0 sb=0 sd=0 mult=1 m=1
XM83 Vg net18 net16 VDD sky130_fd_pr__pfet_01v8 L=4 W=16 nf=1 ad='int((nf+1)/2) * W/nf * 0.29' as='int((nf+2)/2) * W/nf * 0.29'
+ pd='2*int((nf+1)/2) * (W/nf + 0.29)' ps='2*int((nf+2)/2) * (W/nf + 0.29)' nrd='0.29 / W' nrs='0.29 / W'
+ sa=0 sb=0 sd=0 mult=1 m=1
XMdumb45 VDD VDD net18 VDD sky130_fd_pr__pfet_01v8 L=4 W=16 nf=1 ad='int((nf+1)/2) * W/nf * 0.29' as='int((nf+2)/2) * W/nf * 0.29'
+ pd='2*int((nf+1)/2) * (W/nf + 0.29)' ps='2*int((nf+2)/2) * (W/nf + 0.29)' nrd='0.29 / W' nrs='0.29 / W'
+ sa=0 sb=0 sd=0 mult=1 m=1
XMdumb46 VDD VDD net18 VDD sky130_fd_pr__pfet_01v8 L=4 W=16 nf=1 ad='int((nf+1)/2) * W/nf * 0.29' as='int((nf+2)/2) * W/nf * 0.29'
+ pd='2*int((nf+1)/2) * (W/nf + 0.29)' ps='2*int((nf+2)/2) * (W/nf + 0.29)' nrd='0.29 / W' nrs='0.29 / W'
+ sa=0 sb=0 sd=0 mult=1 m=1
XMdumb47 Vg VDD VDD VDD sky130_fd_pr__pfet_01v8 L=4 W=16 nf=1 ad='int((nf+1)/2) * W/nf * 0.29' as='int((nf+2)/2) * W/nf * 0.29'
+ pd='2*int((nf+1)/2) * (W/nf + 0.29)' ps='2*int((nf+2)/2) * (W/nf + 0.29)' nrd='0.29 / W' nrs='0.29 / W'
+ sa=0 sb=0 sd=0 mult=1 m=1
XMdumb48 Vg VDD VDD VDD sky130_fd_pr__pfet_01v8 L=4 W=16 nf=1 ad='int((nf+1)/2) * W/nf * 0.29' as='int((nf+2)/2) * W/nf * 0.29'
+ pd='2*int((nf+1)/2) * (W/nf + 0.29)' ps='2*int((nf+2)/2) * (W/nf + 0.29)' nrd='0.29 / W' nrs='0.29 / W'
+ sa=0 sb=0 sd=0 mult=1 m=1
XMdumb49 GND GND net18 GND sky130_fd_pr__nfet_01v8 L=4 W=16 nf=1 ad='int((nf+1)/2) * W/nf * 0.29' as='int((nf+2)/2) * W/nf * 0.29'
+ pd='2*int((nf+1)/2) * (W/nf + 0.29)' ps='2*int((nf+2)/2) * (W/nf + 0.29)' nrd='0.29 / W' nrs='0.29 / W'
+ sa=0 sb=0 sd=0 mult=1 m=1
XMdumb84 GND GND net18 GND sky130_fd_pr__nfet_01v8 L=4 W=16 nf=1 ad='int((nf+1)/2) * W/nf * 0.29' as='int((nf+2)/2) * W/nf * 0.29'
+ pd='2*int((nf+1)/2) * (W/nf + 0.29)' ps='2*int((nf+2)/2) * (W/nf + 0.29)' nrd='0.29 / W' nrs='0.29 / W'
+ sa=0 sb=0 sd=0 mult=1 m=1
XM51 net18 Vbn net15 GND sky130_fd_pr__nfet_01v8 L=4 W=16 nf=1 ad='int((nf+1)/2) * W/nf * 0.29' as='int((nf+2)/2) * W/nf * 0.29'
+ pd='2*int((nf+1)/2) * (W/nf + 0.29)' ps='2*int((nf+2)/2) * (W/nf + 0.29)' nrd='0.29 / W' nrs='0.29 / W'
+ sa=0 sb=0 sd=0 mult=1 m=1
XM52 net18 Vbn net15 GND sky130_fd_pr__nfet_01v8 L=4 W=16 nf=1 ad='int((nf+1)/2) * W/nf * 0.29' as='int((nf+2)/2) * W/nf * 0.29'
+ pd='2*int((nf+1)/2) * (W/nf + 0.29)' ps='2*int((nf+2)/2) * (W/nf + 0.29)' nrd='0.29 / W' nrs='0.29 / W'
+ sa=0 sb=0 sd=0 mult=1 m=1
XM53 net15 Vbn GND GND sky130_fd_pr__nfet_01v8 L=4 W=16 nf=1 ad='int((nf+1)/2) * W/nf * 0.29' as='int((nf+2)/2) * W/nf * 0.29'
+ pd='2*int((nf+1)/2) * (W/nf + 0.29)' ps='2*int((nf+2)/2) * (W/nf + 0.29)' nrd='0.29 / W' nrs='0.29 / W'
+ sa=0 sb=0 sd=0 mult=1 m=1
XM54 net15 Vbn GND GND sky130_fd_pr__nfet_01v8 L=4 W=16 nf=1 ad='int((nf+1)/2) * W/nf * 0.29' as='int((nf+2)/2) * W/nf * 0.29'
+ pd='2*int((nf+1)/2) * (W/nf + 0.29)' ps='2*int((nf+2)/2) * (W/nf + 0.29)' nrd='0.29 / W' nrs='0.29 / W'
+ sa=0 sb=0 sd=0 mult=1 m=1
XM55 GND net9 net17 GND sky130_fd_pr__nfet_01v8 L=4 W=16 nf=1 ad='int((nf+1)/2) * W/nf * 0.29' as='int((nf+2)/2) * W/nf * 0.29'
+ pd='2*int((nf+1)/2) * (W/nf + 0.29)' ps='2*int((nf+2)/2) * (W/nf + 0.29)' nrd='0.29 / W' nrs='0.29 / W'
+ sa=0 sb=0 sd=0 mult=1 m=1
XM56 net17 net9 GND GND sky130_fd_pr__nfet_01v8 L=4 W=16 nf=1 ad='int((nf+1)/2) * W/nf * 0.29' as='int((nf+2)/2) * W/nf * 0.29'
+ pd='2*int((nf+1)/2) * (W/nf + 0.29)' ps='2*int((nf+2)/2) * (W/nf + 0.29)' nrd='0.29 / W' nrs='0.29 / W'
+ sa=0 sb=0 sd=0 mult=1 m=1
XM57 net17 net9 Vg GND sky130_fd_pr__nfet_01v8 L=4 W=16 nf=1 ad='int((nf+1)/2) * W/nf * 0.29' as='int((nf+2)/2) * W/nf * 0.29'
+ pd='2*int((nf+1)/2) * (W/nf + 0.29)' ps='2*int((nf+2)/2) * (W/nf + 0.29)' nrd='0.29 / W' nrs='0.29 / W'
+ sa=0 sb=0 sd=0 mult=1 m=1
XM58 Vg net9 net17 GND sky130_fd_pr__nfet_01v8 L=4 W=16 nf=1 ad='int((nf+1)/2) * W/nf * 0.29' as='int((nf+2)/2) * W/nf * 0.29'
+ pd='2*int((nf+1)/2) * (W/nf + 0.29)' ps='2*int((nf+2)/2) * (W/nf + 0.29)' nrd='0.29 / W' nrs='0.29 / W'
+ sa=0 sb=0 sd=0 mult=1 m=1
XMdumb85 Vg GND GND GND sky130_fd_pr__nfet_01v8 L=4 W=16 nf=1 ad='int((nf+1)/2) * W/nf * 0.29' as='int((nf+2)/2) * W/nf * 0.29'
+ pd='2*int((nf+1)/2) * (W/nf + 0.29)' ps='2*int((nf+2)/2) * (W/nf + 0.29)' nrd='0.29 / W' nrs='0.29 / W'
+ sa=0 sb=0 sd=0 mult=1 m=1
XMdumb60 Vg GND GND GND sky130_fd_pr__nfet_01v8 L=4 W=16 nf=1 ad='int((nf+1)/2) * W/nf * 0.29' as='int((nf+2)/2) * W/nf * 0.29'
+ pd='2*int((nf+1)/2) * (W/nf + 0.29)' ps='2*int((nf+2)/2) * (W/nf + 0.29)' nrd='0.29 / W' nrs='0.29 / W'
+ sa=0 sb=0 sd=0 mult=1 m=1
**.ends
.GLOBAL GND
.GLOBAL VDD
.end
